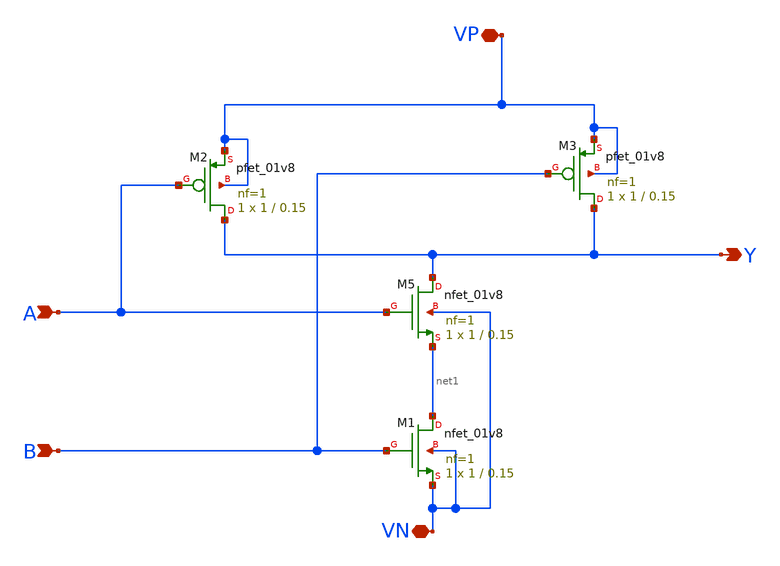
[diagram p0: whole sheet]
** sch_path: nand.sch
**.subckt nand Y VP VN A B
*.opin Y
*.iopin VP
*.iopin VN
*.ipin A
*.ipin B
XM5 Y A net1 VN sky130_fd_pr__nfet_01v8 L=0.15 W=1 nf=1 ad='int((nf+1)/2) * W/nf * 0.29' as='int((nf+2)/2) * W/nf * 0.29'
+ pd='2*int((nf+1)/2) * (W/nf + 0.29)' ps='2*int((nf+2)/2) * (W/nf + 0.29)' nrd='0.29 / W' nrs='0.29 / W'
+ sa=0 sb=0 sd=0 mult=1 m=1
XM1 net1 B VN VN sky130_fd_pr__nfet_01v8 L=0.15 W=1 nf=1 ad='int((nf+1)/2) * W/nf * 0.29' as='int((nf+2)/2) * W/nf * 0.29'
+ pd='2*int((nf+1)/2) * (W/nf + 0.29)' ps='2*int((nf+2)/2) * (W/nf + 0.29)' nrd='0.29 / W' nrs='0.29 / W'
+ sa=0 sb=0 sd=0 mult=1 m=1
XM2 Y A VP VP sky130_fd_pr__pfet_01v8 L=0.15 W=1 nf=1 ad='int((nf+1)/2) * W/nf * 0.29' as='int((nf+2)/2) * W/nf * 0.29'
+ pd='2*int((nf+1)/2) * (W/nf + 0.29)' ps='2*int((nf+2)/2) * (W/nf + 0.29)' nrd='0.29 / W' nrs='0.29 / W'
+ sa=0 sb=0 sd=0 mult=1 m=1
XM3 Y B VP VP sky130_fd_pr__pfet_01v8 L=0.15 W=1 nf=1 ad='int((nf+1)/2) * W/nf * 0.29' as='int((nf+2)/2) * W/nf * 0.29'
+ pd='2*int((nf+1)/2) * (W/nf + 0.29)' ps='2*int((nf+2)/2) * (W/nf + 0.29)' nrd='0.29 / W' nrs='0.29 / W'
+ sa=0 sb=0 sd=0 mult=1 m=1
**.ends
.end
